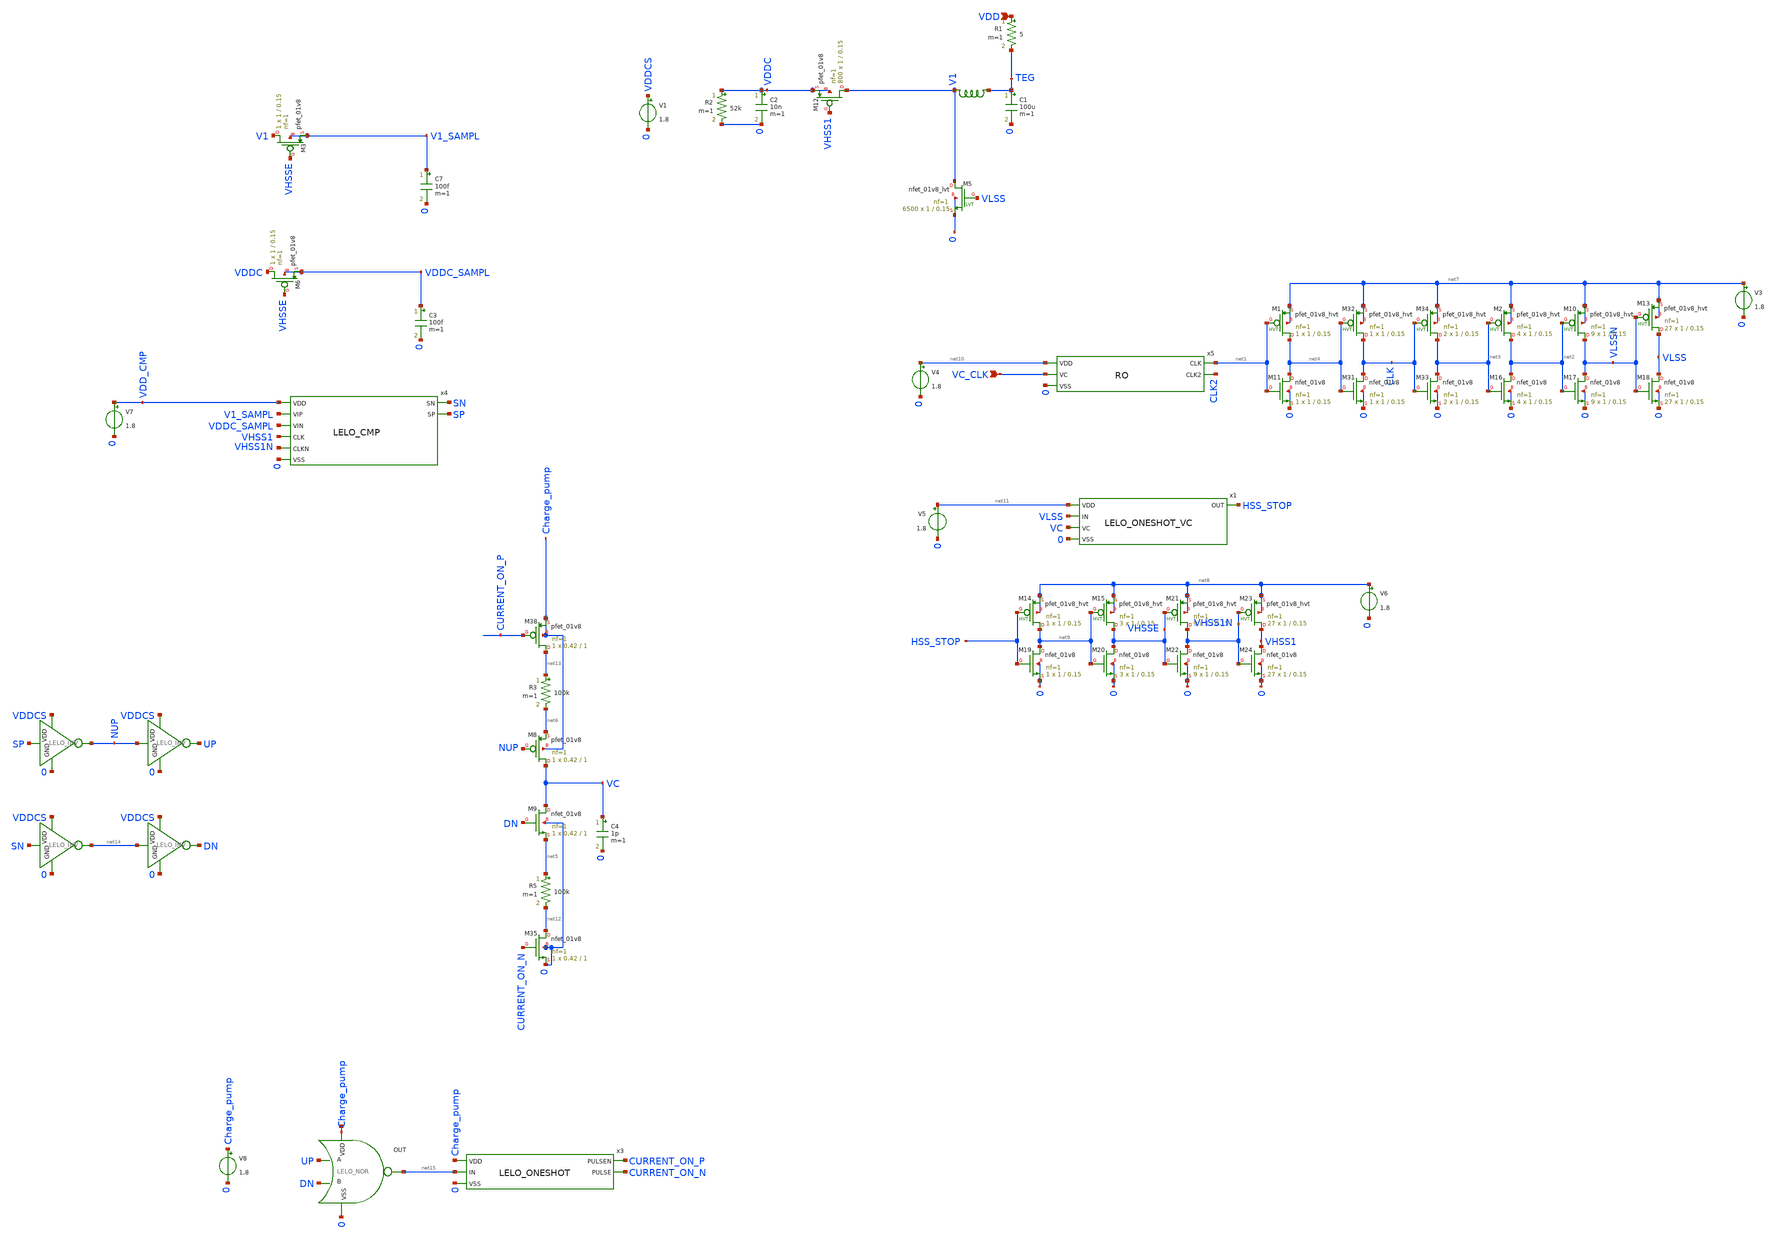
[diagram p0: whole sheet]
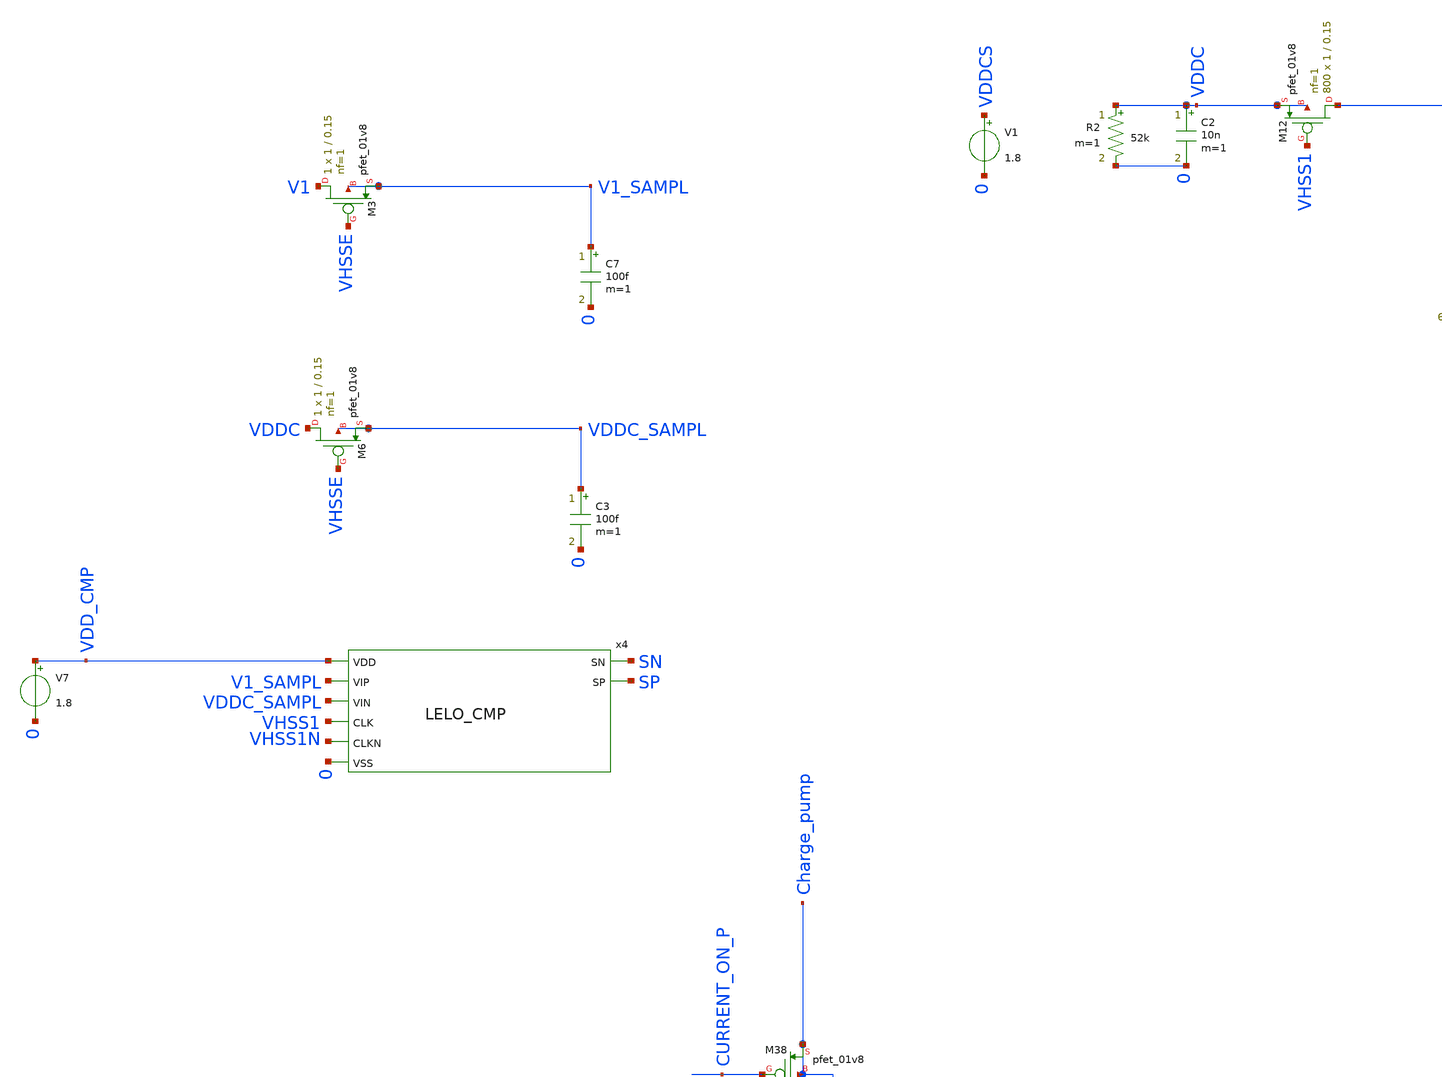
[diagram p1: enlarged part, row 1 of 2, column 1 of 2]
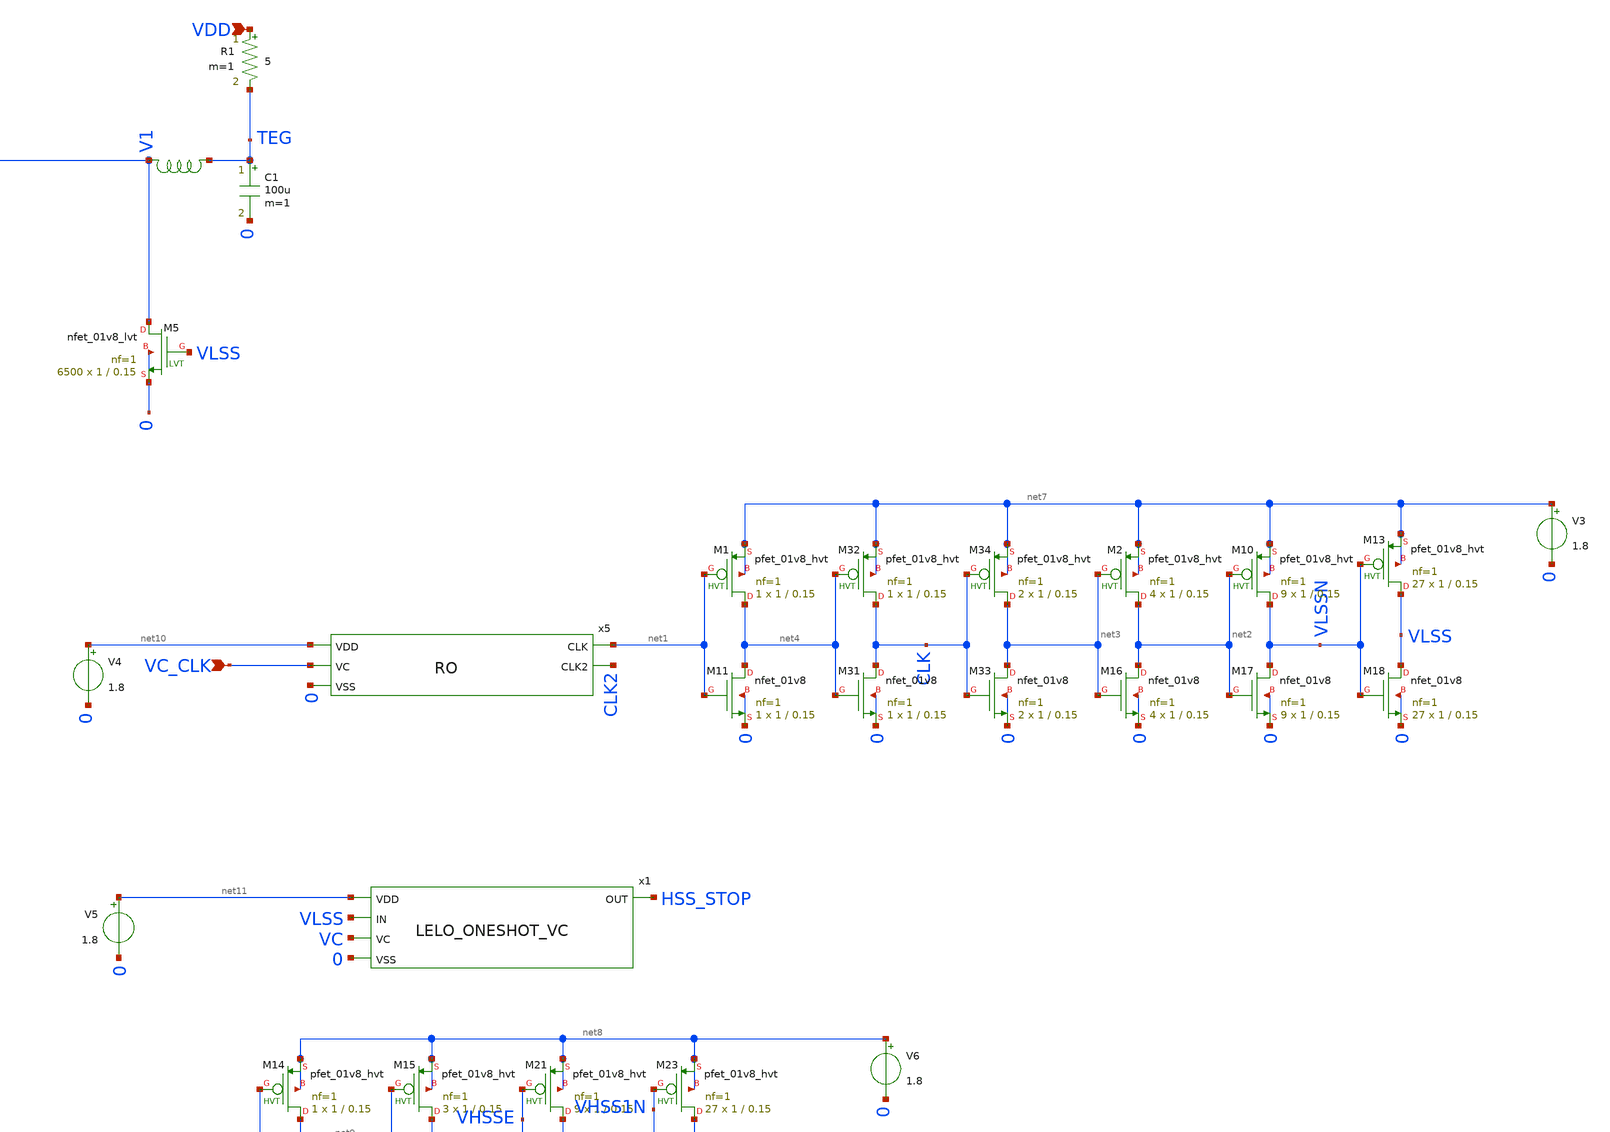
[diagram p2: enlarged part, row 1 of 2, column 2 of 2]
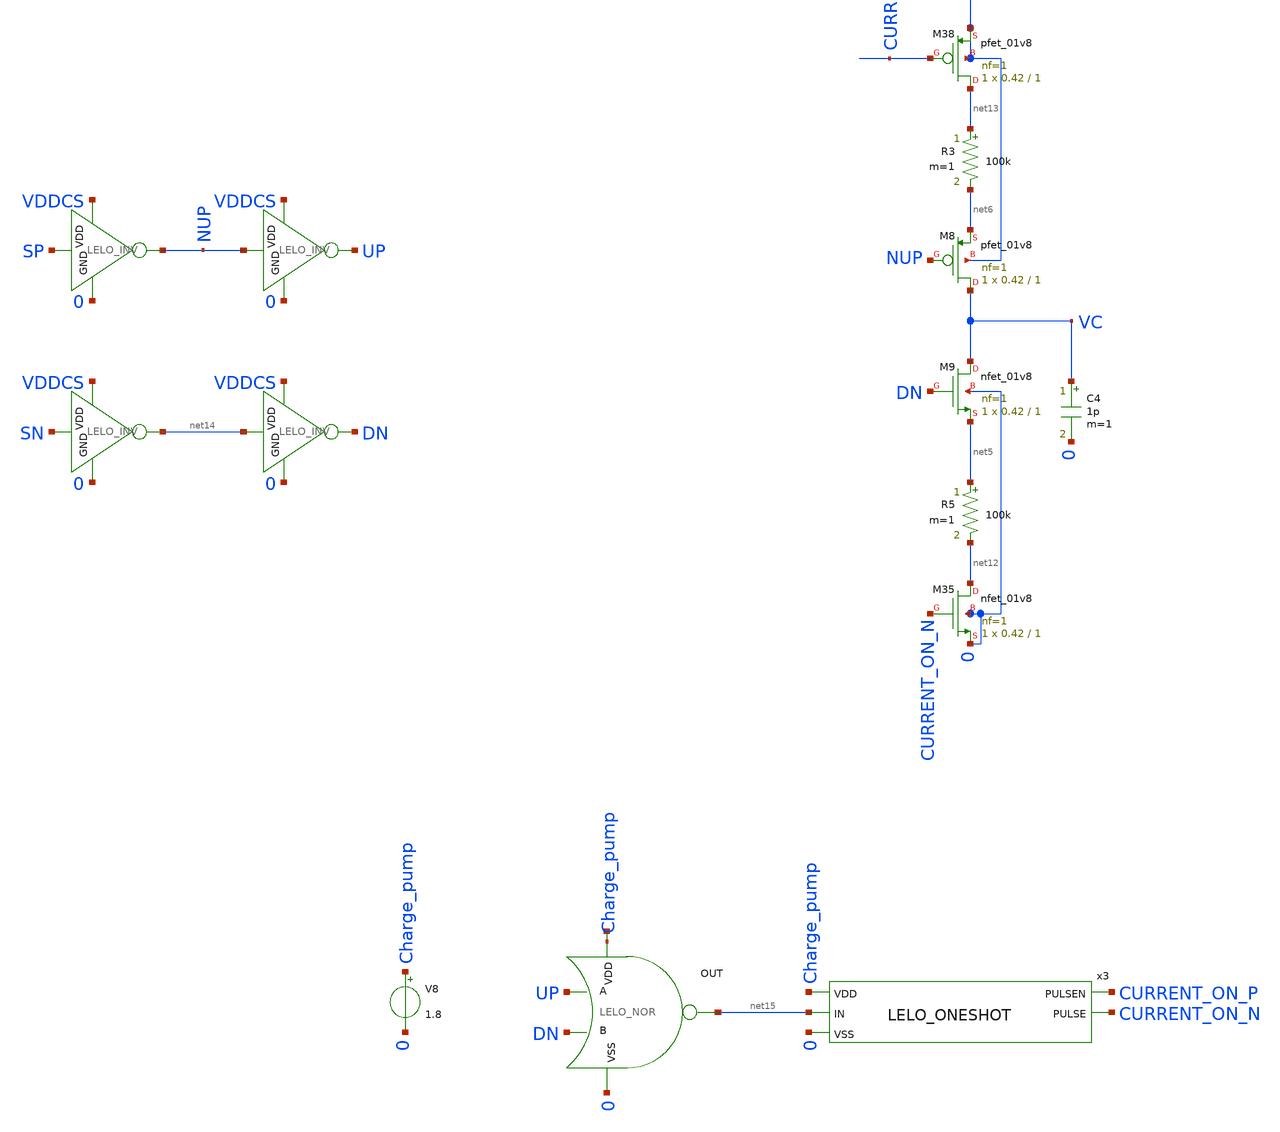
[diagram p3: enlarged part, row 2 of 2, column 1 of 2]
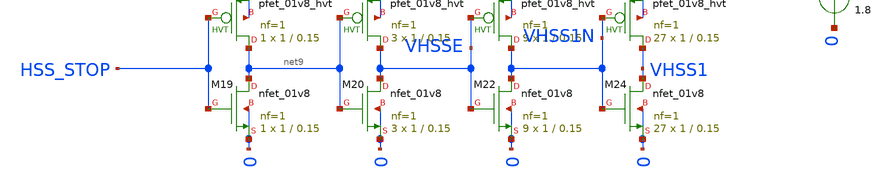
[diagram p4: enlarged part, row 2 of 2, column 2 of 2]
** sch_path: design/LELO_SVOD_SKY130A/LELO_BOOST_STEADY_STATE.sch
**.subckt LELO_BOOST_STEADY_STATE VDD VC_CLK
*.ipin VDD
*.ipin VC_CLK
R1 VDD TEG 5 m=1
C7 V1_SAMPL 0 100f m=1
x5 net1 CLK2 net10 VC_CLK 0 RO
XM12 V1 VHSS1 VDDC VDDC sky130_fd_pr__pfet_01v8 L=0.15 W=1 nf=1 ad='int((1 + 1)/2) * 1 / 1 * 0.29' as='int((1 + 2)/2) * 1 / 1 * 0.29'
+ pd='2*int((1 + 1)/2) * (1 / 1 + 0.29)' ps='2*int((1 + 2)/2) * (1 / 1 + 0.29)' nrd='0.29 / 1 ' nrs='0.29 / 1 '
+ sa=0 sb=0 sd=0 mult=800 m=800
C1 TEG 0 100u m=1
XM5 V1 VLSS 0 0 sky130_fd_pr__nfet_01v8_lvt L=0.15 W=1 nf=1 ad='int((1 + 1)/2) * 1 / 1 * 0.29' as='int((1 + 2)/2) * 1 / 1 * 0.29'
+ pd='2*int((1 + 1)/2) * (1 / 1 + 0.29)' ps='2*int((1 + 2)/2) * (1 / 1 + 0.29)' nrd='0.29 / 1 ' nrs='0.29 / 1 '
+ sa=0 sb=0 sd=0 mult=6500 m=6500
C2 VDDC 0 10n m=1
V1 VDDCS 0 1.8
R2 VDDC 0 52k m=1
x4 SN SP VDD_CMP V1_SAMPL VDDC_SAMPL VHSS1 VHSS1N 0 LELO_CMP
XM3 V1 VHSSE V1_SAMPL V1_SAMPL sky130_fd_pr__pfet_01v8 L=0.15 W=1 nf=1 ad='int((1 + 1)/2) * 1 / 1 * 0.29'
+ as='int((1 + 2)/2) * 1 / 1 * 0.29' pd='2*int((1 + 1)/2) * (1 / 1 + 0.29)' ps='2*int((1 + 2)/2) * (1 / 1 + 0.29)'
+ nrd='0.29 / 1 ' nrs='0.29 / 1 ' sa=0 sb=0 sd=0 mult=1 m=1
C3 VDDC_SAMPL 0 100f m=1
XM6 VDDC VHSSE VDDC_SAMPL VDDC_SAMPL sky130_fd_pr__pfet_01v8 L=0.15 W=1 nf=1 ad='int((1 + 1)/2) * 1 / 1 * 0.29'
+ as='int((1 + 2)/2) * 1 / 1 * 0.29' pd='2*int((1 + 1)/2) * (1 / 1 + 0.29)' ps='2*int((1 + 2)/2) * (1 / 1 + 0.29)'
+ nrd='0.29 / 1 ' nrs='0.29 / 1 ' sa=0 sb=0 sd=0 mult=1 m=1
C4 VC 0 1p m=1
XM8 VC NUP net6 Charge_pump sky130_fd_pr__pfet_01v8 L=1 W=0.42 nf=1 ad='int((1 + 1)/2) * 0.42 / 1 * 0.29'
+ as='int((1 + 2)/2) * 0.42 / 1 * 0.29' pd='2*int((1 + 1)/2) * (0.42 / 1 + 0.29)' ps='2*int((1 + 2)/2) * (0.42 / 1 + 0.29)'
+ nrd='0.29 / 0.42 ' nrs='0.29 / 0.42 ' sa=0 sb=0 sd=0 mult=1 m=1
XM9 VC DN net5 0 sky130_fd_pr__nfet_01v8 L=1 W=0.42 nf=1 ad='int((1 + 1)/2) * 0.42 / 1 * 0.29' as='int((1 + 2)/2) * 0.42 / 1 * 0.29'
+ pd='2*int((1 + 1)/2) * (0.42 / 1 + 0.29)' ps='2*int((1 + 2)/2) * (0.42 / 1 + 0.29)' nrd='0.29 / 0.42 '
+ nrs='0.29 / 0.42 ' sa=0 sb=0 sd=0 mult=1 m=1
XM11 net4 net1 0 0 sky130_fd_pr__nfet_01v8 L=0.15 W=1 nf=1 ad='int((1 + 1)/2) * 1 / 1 * 0.29' as='int((1 + 2)/2) * 1 / 1 * 0.29'
+ pd='2*int((1 + 1)/2) * (1 / 1 + 0.29)' ps='2*int((1 + 2)/2) * (1 / 1 + 0.29)' nrd='0.29 / 1 ' nrs='0.29 / 1 '
+ sa=0 sb=0 sd=0 mult=1 m=1
XM16 net2 net3 0 0 sky130_fd_pr__nfet_01v8 L=0.15 W=1 nf=1 ad='int((1 + 1)/2) * 1 / 1 * 0.29' as='int((1 + 2)/2) * 1 / 1 * 0.29'
+ pd='2*int((1 + 1)/2) * (1 / 1 + 0.29)' ps='2*int((1 + 2)/2) * (1 / 1 + 0.29)' nrd='0.29 / 1 ' nrs='0.29 / 1 '
+ sa=0 sb=0 sd=0 mult=4 m=4
XM17 VLSSN net2 0 0 sky130_fd_pr__nfet_01v8 L=0.15 W=1 nf=1 ad='int((1 + 1)/2) * 1 / 1 * 0.29' as='int((1 + 2)/2) * 1 / 1 * 0.29'
+ pd='2*int((1 + 1)/2) * (1 / 1 + 0.29)' ps='2*int((1 + 2)/2) * (1 / 1 + 0.29)' nrd='0.29 / 1 ' nrs='0.29 / 1 '
+ sa=0 sb=0 sd=0 mult=9 m=9
XM18 VLSS VLSSN 0 0 sky130_fd_pr__nfet_01v8 L=0.15 W=1 nf=1 ad='int((1 + 1)/2) * 1 / 1 * 0.29' as='int((1 + 2)/2) * 1 / 1 * 0.29'
+ pd='2*int((1 + 1)/2) * (1 / 1 + 0.29)' ps='2*int((1 + 2)/2) * (1 / 1 + 0.29)' nrd='0.29 / 1 ' nrs='0.29 / 1 '
+ sa=0 sb=0 sd=0 mult=27 m=27
XM19 net9 HSS_STOP 0 0 sky130_fd_pr__nfet_01v8 L=0.15 W=1 nf=1 ad='int((1 + 1)/2) * 1 / 1 * 0.29' as='int((1 + 2)/2) * 1 / 1 * 0.29'
+ pd='2*int((1 + 1)/2) * (1 / 1 + 0.29)' ps='2*int((1 + 2)/2) * (1 / 1 + 0.29)' nrd='0.29 / 1 ' nrs='0.29 / 1 '
+ sa=0 sb=0 sd=0 mult=1 m=1
XM20 VHSSE net9 0 0 sky130_fd_pr__nfet_01v8 L=0.15 W=1 nf=1 ad='int((1 + 1)/2) * 1 / 1 * 0.29' as='int((1 + 2)/2) * 1 / 1 * 0.29'
+ pd='2*int((1 + 1)/2) * (1 / 1 + 0.29)' ps='2*int((1 + 2)/2) * (1 / 1 + 0.29)' nrd='0.29 / 1 ' nrs='0.29 / 1 '
+ sa=0 sb=0 sd=0 mult=3 m=3
XM22 VHSS1N VHSSE 0 0 sky130_fd_pr__nfet_01v8 L=0.15 W=1 nf=1 ad='int((1 + 1)/2) * 1 / 1 * 0.29' as='int((1 + 2)/2) * 1 / 1 * 0.29'
+ pd='2*int((1 + 1)/2) * (1 / 1 + 0.29)' ps='2*int((1 + 2)/2) * (1 / 1 + 0.29)' nrd='0.29 / 1 ' nrs='0.29 / 1 '
+ sa=0 sb=0 sd=0 mult=9 m=9
XM24 VHSS1 VHSS1N 0 0 sky130_fd_pr__nfet_01v8 L=0.15 W=1 nf=1 ad='int((1 + 1)/2) * 1 / 1 * 0.29' as='int((1 + 2)/2) * 1 / 1 * 0.29'
+ pd='2*int((1 + 1)/2) * (1 / 1 + 0.29)' ps='2*int((1 + 2)/2) * (1 / 1 + 0.29)' nrd='0.29 / 1 ' nrs='0.29 / 1 '
+ sa=0 sb=0 sd=0 mult=27 m=27
XM1 net4 net1 net7 net7 sky130_fd_pr__pfet_01v8_hvt L=0.15 W=1 nf=1 ad='int((1 + 1)/2) * 1 / 1 * 0.29'
+ as='int((1 + 2)/2) * 1 / 1 * 0.29' pd='2*int((1 + 1)/2) * (1 / 1 + 0.29)' ps='2*int((1 + 2)/2) * (1 / 1 + 0.29)'
+ nrd='0.29 / 1 ' nrs='0.29 / 1 ' sa=0 sb=0 sd=0 mult=1 m=1
XM2 net2 net3 net7 net7 sky130_fd_pr__pfet_01v8_hvt L=0.15 W=1 nf=1 ad='int((1 + 1)/2) * 1 / 1 * 0.29'
+ as='int((1 + 2)/2) * 1 / 1 * 0.29' pd='2*int((1 + 1)/2) * (1 / 1 + 0.29)' ps='2*int((1 + 2)/2) * (1 / 1 + 0.29)'
+ nrd='0.29 / 1 ' nrs='0.29 / 1 ' sa=0 sb=0 sd=0 mult=4 m=4
XM10 VLSSN net2 net7 net7 sky130_fd_pr__pfet_01v8_hvt L=0.15 W=1 nf=1 ad='int((1 + 1)/2) * 1 / 1 * 0.29'
+ as='int((1 + 2)/2) * 1 / 1 * 0.29' pd='2*int((1 + 1)/2) * (1 / 1 + 0.29)' ps='2*int((1 + 2)/2) * (1 / 1 + 0.29)'
+ nrd='0.29 / 1 ' nrs='0.29 / 1 ' sa=0 sb=0 sd=0 mult=9 m=9
XM13 VLSS VLSSN net7 net7 sky130_fd_pr__pfet_01v8_hvt L=0.15 W=1 nf=1 ad='int((1 + 1)/2) * 1 / 1 * 0.29'
+ as='int((1 + 2)/2) * 1 / 1 * 0.29' pd='2*int((1 + 1)/2) * (1 / 1 + 0.29)' ps='2*int((1 + 2)/2) * (1 / 1 + 0.29)'
+ nrd='0.29 / 1 ' nrs='0.29 / 1 ' sa=0 sb=0 sd=0 mult=27 m=27
XM14 net9 HSS_STOP net8 net8 sky130_fd_pr__pfet_01v8_hvt L=0.15 W=1 nf=1 ad='int((1 + 1)/2) * 1 / 1 * 0.29'
+ as='int((1 + 2)/2) * 1 / 1 * 0.29' pd='2*int((1 + 1)/2) * (1 / 1 + 0.29)' ps='2*int((1 + 2)/2) * (1 / 1 + 0.29)'
+ nrd='0.29 / 1 ' nrs='0.29 / 1 ' sa=0 sb=0 sd=0 mult=1 m=1
XM15 VHSSE net9 net8 net8 sky130_fd_pr__pfet_01v8_hvt L=0.15 W=1 nf=1 ad='int((1 + 1)/2) * 1 / 1 * 0.29'
+ as='int((1 + 2)/2) * 1 / 1 * 0.29' pd='2*int((1 + 1)/2) * (1 / 1 + 0.29)' ps='2*int((1 + 2)/2) * (1 / 1 + 0.29)'
+ nrd='0.29 / 1 ' nrs='0.29 / 1 ' sa=0 sb=0 sd=0 mult=3 m=3
XM21 VHSS1N VHSSE net8 net8 sky130_fd_pr__pfet_01v8_hvt L=0.15 W=1 nf=1 ad='int((1 + 1)/2) * 1 / 1 * 0.29'
+ as='int((1 + 2)/2) * 1 / 1 * 0.29' pd='2*int((1 + 1)/2) * (1 / 1 + 0.29)' ps='2*int((1 + 2)/2) * (1 / 1 + 0.29)'
+ nrd='0.29 / 1 ' nrs='0.29 / 1 ' sa=0 sb=0 sd=0 mult=9 m=9
XM23 VHSS1 VHSS1N net8 net8 sky130_fd_pr__pfet_01v8_hvt L=0.15 W=1 nf=1 ad='int((1 + 1)/2) * 1 / 1 * 0.29'
+ as='int((1 + 2)/2) * 1 / 1 * 0.29' pd='2*int((1 + 1)/2) * (1 / 1 + 0.29)' ps='2*int((1 + 2)/2) * (1 / 1 + 0.29)'
+ nrd='0.29 / 1 ' nrs='0.29 / 1 ' sa=0 sb=0 sd=0 mult=27 m=27
V4 net10 0 1.8
V3 net7 0 1.8
V5 net11 0 1.8
V6 net8 0 1.8
V7 VDD_CMP 0 1.8
XM31 CLK net4 0 0 sky130_fd_pr__nfet_01v8 L=0.15 W=1 nf=1 ad='int((1 + 1)/2) * 1 / 1 * 0.29' as='int((1 + 2)/2) * 1 / 1 * 0.29'
+ pd='2*int((1 + 1)/2) * (1 / 1 + 0.29)' ps='2*int((1 + 2)/2) * (1 / 1 + 0.29)' nrd='0.29 / 1 ' nrs='0.29 / 1 '
+ sa=0 sb=0 sd=0 mult=1 m=1
XM32 CLK net4 net7 net7 sky130_fd_pr__pfet_01v8_hvt L=0.15 W=1 nf=1 ad='int((1 + 1)/2) * 1 / 1 * 0.29'
+ as='int((1 + 2)/2) * 1 / 1 * 0.29' pd='2*int((1 + 1)/2) * (1 / 1 + 0.29)' ps='2*int((1 + 2)/2) * (1 / 1 + 0.29)'
+ nrd='0.29 / 1 ' nrs='0.29 / 1 ' sa=0 sb=0 sd=0 mult=1 m=1
XM33 net3 CLK 0 0 sky130_fd_pr__nfet_01v8 L=0.15 W=1 nf=1 ad='int((1 + 1)/2) * 1 / 1 * 0.29' as='int((1 + 2)/2) * 1 / 1 * 0.29'
+ pd='2*int((1 + 1)/2) * (1 / 1 + 0.29)' ps='2*int((1 + 2)/2) * (1 / 1 + 0.29)' nrd='0.29 / 1 ' nrs='0.29 / 1 '
+ sa=0 sb=0 sd=0 mult=2 m=2
XM34 net3 CLK net7 net7 sky130_fd_pr__pfet_01v8_hvt L=0.15 W=1 nf=1 ad='int((1 + 1)/2) * 1 / 1 * 0.29'
+ as='int((1 + 2)/2) * 1 / 1 * 0.29' pd='2*int((1 + 1)/2) * (1 / 1 + 0.29)' ps='2*int((1 + 2)/2) * (1 / 1 + 0.29)'
+ nrd='0.29 / 1 ' nrs='0.29 / 1 ' sa=0 sb=0 sd=0 mult=2 m=2
x7 TEG V1 XGL6030-822_sat
x10 VDDCS SP NUP 0 LELO_INV
R5 net5 net12 100k m=1
XM35 net12 CURRENT_ON_N 0 0 sky130_fd_pr__nfet_01v8 L=1 W=0.42 nf=1 ad='int((1 + 1)/2) * 0.42 / 1 * 0.29'
+ as='int((1 + 2)/2) * 0.42 / 1 * 0.29' pd='2*int((1 + 1)/2) * (0.42 / 1 + 0.29)' ps='2*int((1 + 2)/2) * (0.42 / 1 + 0.29)'
+ nrd='0.29 / 0.42 ' nrs='0.29 / 0.42 ' sa=0 sb=0 sd=0 mult=1 m=1
XM38 net13 CURRENT_ON_P Charge_pump Charge_pump sky130_fd_pr__pfet_01v8 L=1 W=0.42 nf=1 ad='int((1 + 1)/2) * 0.42 / 1 * 0.29'
+ as='int((1 + 2)/2) * 0.42 / 1 * 0.29' pd='2*int((1 + 1)/2) * (0.42 / 1 + 0.29)' ps='2*int((1 + 2)/2) * (0.42 / 1 + 0.29)'
+ nrd='0.29 / 0.42 ' nrs='0.29 / 0.42 ' sa=0 sb=0 sd=0 mult=1 m=1
V8 Charge_pump 0 1.8
x11 VDDCS SN net14 0 LELO_INV
x14 VDDCS net14 DN 0 LELO_INV
x17 VDDCS NUP UP 0 LELO_INV
x1 net11 VLSS VC HSS_STOP 0 LELO_ONESHOT_VC
x2 net16 net15 UP DN 0 LELO_NOR
x3 Charge_pump net15 0 CURRENT_ON_P CURRENT_ON_N LELO_ONESHOT
R3 net13 net6 100k m=1
**.ends
.end
